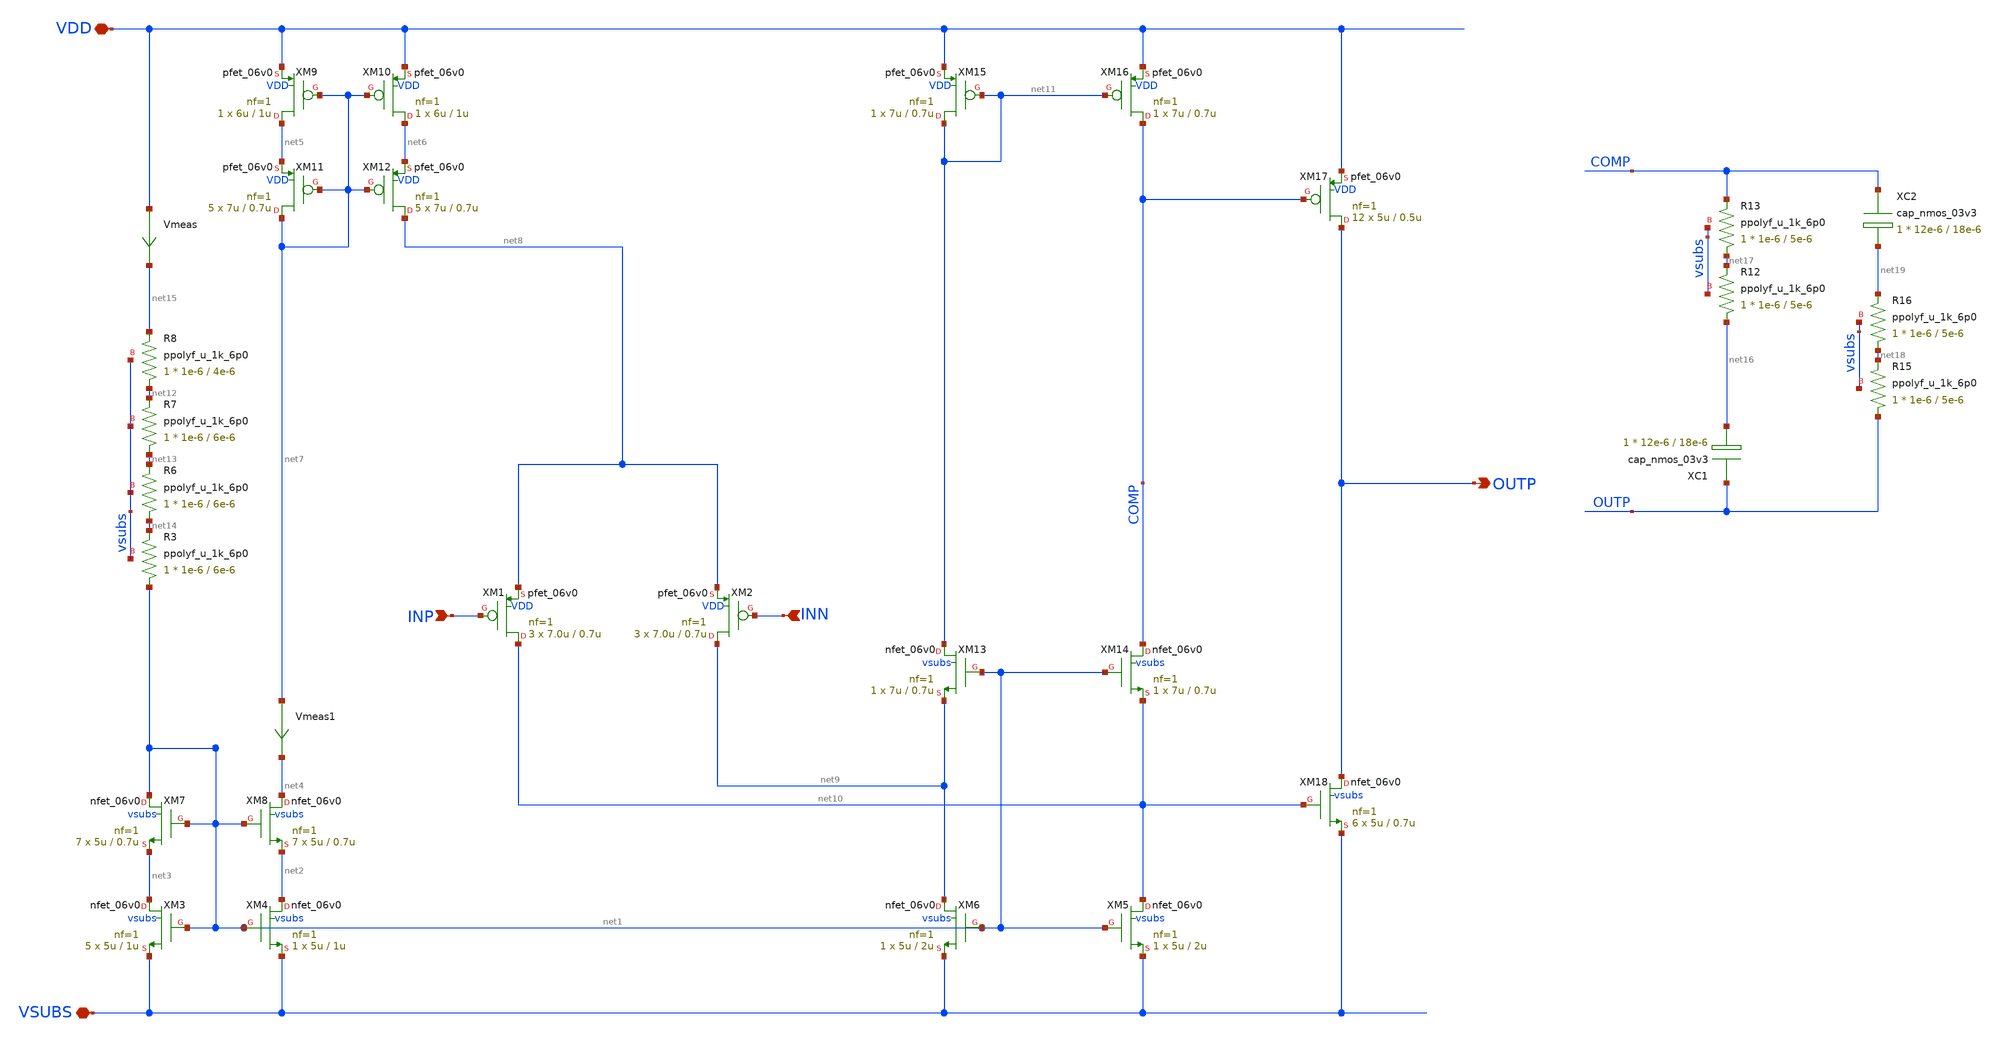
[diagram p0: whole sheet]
** sch_path: xschem/ip_amplifier.sch
**.subckt ip_amplifier VDD VSUBS INP INN OUTP
*.iopin VDD
*.iopin VSUBS
*.ipin INP
*.ipin INN
*.opin OUTP
XM1 net10 INP net8 VDD pfet_06v0 L=0.7u W=7.0u nf=1 ad='int((nf+1)/2) * W/nf * 0.18u' as='int((nf+2)/2) * W/nf * 0.18u'
+ pd='2*int((nf+1)/2) * (W/nf + 0.18u)' ps='2*int((nf+2)/2) * (W/nf + 0.18u)' nrd='0.18u / W' nrs='0.18u / W'
+ sa=0 sb=0 sd=0 m=3 par=3
XM2 net9 INN net8 VDD pfet_06v0 L=0.7u W=7.0u nf=1 ad='int((nf+1)/2) * W/nf * 0.18u' as='int((nf+2)/2) * W/nf * 0.18u'
+ pd='2*int((nf+1)/2) * (W/nf + 0.18u)' ps='2*int((nf+2)/2) * (W/nf + 0.18u)' nrd='0.18u / W' nrs='0.18u / W'
+ sa=0 sb=0 sd=0 m=3 par=3
XM5 net10 net1 VSUBS vsubs nfet_06v0 L=2u W=5u nf=1 ad='int((nf+1)/2) * W/nf * 0.18u' as='int((nf+2)/2) * W/nf * 0.18u'
+ pd='2*int((nf+1)/2) * (W/nf + 0.18u)' ps='2*int((nf+2)/2) * (W/nf + 0.18u)' nrd='0.18u / W' nrs='0.18u / W'
+ sa=0 sb=0 sd=0 m=1 par=1
XM6 net9 net1 VSUBS vsubs nfet_06v0 L=2u W=5u nf=1 ad='int((nf+1)/2) * W/nf * 0.18u' as='int((nf+2)/2) * W/nf * 0.18u'
+ pd='2*int((nf+1)/2) * (W/nf + 0.18u)' ps='2*int((nf+2)/2) * (W/nf + 0.18u)' nrd='0.18u / W' nrs='0.18u / W'
+ sa=0 sb=0 sd=0 m=1 par=1
XM3 net3 net1 VSUBS vsubs nfet_06v0 L=1u W=5u nf=1 ad='int((nf+1)/2) * W/nf * 0.18u' as='int((nf+2)/2) * W/nf * 0.18u'
+ pd='2*int((nf+1)/2) * (W/nf + 0.18u)' ps='2*int((nf+2)/2) * (W/nf + 0.18u)' nrd='0.18u / W' nrs='0.18u / W'
+ sa=0 sb=0 sd=0 m=5 par=5
XM4 net2 net1 VSUBS vsubs nfet_06v0 L=1u W=5u nf=1 ad='int((nf+1)/2) * W/nf * 0.18u' as='int((nf+2)/2) * W/nf * 0.18u'
+ pd='2*int((nf+1)/2) * (W/nf + 0.18u)' ps='2*int((nf+2)/2) * (W/nf + 0.18u)' nrd='0.18u / W' nrs='0.18u / W'
+ sa=0 sb=0 sd=0 m=1 par=1
XM7 net1 net1 net3 vsubs nfet_06v0 L=0.7u W=5u nf=1 ad='int((nf+1)/2) * W/nf * 0.18u' as='int((nf+2)/2) * W/nf * 0.18u'
+ pd='2*int((nf+1)/2) * (W/nf + 0.18u)' ps='2*int((nf+2)/2) * (W/nf + 0.18u)' nrd='0.18u / W' nrs='0.18u / W'
+ sa=0 sb=0 sd=0 m=7 par=7
XM8 net4 net1 net2 vsubs nfet_06v0 L=0.7u W=5u nf=1 ad='int((nf+1)/2) * W/nf * 0.18u' as='int((nf+2)/2) * W/nf * 0.18u'
+ pd='2*int((nf+1)/2) * (W/nf + 0.18u)' ps='2*int((nf+2)/2) * (W/nf + 0.18u)' nrd='0.18u / W' nrs='0.18u / W'
+ sa=0 sb=0 sd=0 m=7 par=7
XM9 net5 net7 VDD VDD pfet_06v0 L=1u W=6u nf=1 ad='int((nf+1)/2) * W/nf * 0.18u' as='int((nf+2)/2) * W/nf * 0.18u'
+ pd='2*int((nf+1)/2) * (W/nf + 0.18u)' ps='2*int((nf+2)/2) * (W/nf + 0.18u)' nrd='0.18u / W' nrs='0.18u / W'
+ sa=0 sb=0 sd=0 m=1 par=1
XM10 net6 net7 VDD VDD pfet_06v0 L=1u W=6u nf=1 ad='int((nf+1)/2) * W/nf * 0.18u' as='int((nf+2)/2) * W/nf * 0.18u'
+ pd='2*int((nf+1)/2) * (W/nf + 0.18u)' ps='2*int((nf+2)/2) * (W/nf + 0.18u)' nrd='0.18u / W' nrs='0.18u / W'
+ sa=0 sb=0 sd=0 m=1 par=1
XM11 net7 net7 net5 VDD pfet_06v0 L=0.7u W=7u nf=1 ad='int((nf+1)/2) * W/nf * 0.18u' as='int((nf+2)/2) * W/nf * 0.18u'
+ pd='2*int((nf+1)/2) * (W/nf + 0.18u)' ps='2*int((nf+2)/2) * (W/nf + 0.18u)' nrd='0.18u / W' nrs='0.18u / W'
+ sa=0 sb=0 sd=0 m=5 par=5
XM12 net8 net7 net6 VDD pfet_06v0 L=0.7u W=7u nf=1 ad='int((nf+1)/2) * W/nf * 0.18u' as='int((nf+2)/2) * W/nf * 0.18u'
+ pd='2*int((nf+1)/2) * (W/nf + 0.18u)' ps='2*int((nf+2)/2) * (W/nf + 0.18u)' nrd='0.18u / W' nrs='0.18u / W'
+ sa=0 sb=0 sd=0 m=5 par=5
XM13 net11 net1 net9 vsubs nfet_06v0 L=0.7u W=7u nf=1 ad='int((nf+1)/2) * W/nf * 0.18u' as='int((nf+2)/2) * W/nf * 0.18u'
+ pd='2*int((nf+1)/2) * (W/nf + 0.18u)' ps='2*int((nf+2)/2) * (W/nf + 0.18u)' nrd='0.18u / W' nrs='0.18u / W'
+ sa=0 sb=0 sd=0 m=1 par=1
XM14 COMP net1 net10 vsubs nfet_06v0 L=0.7u W=7u nf=1 ad='int((nf+1)/2) * W/nf * 0.18u' as='int((nf+2)/2) * W/nf * 0.18u'
+ pd='2*int((nf+1)/2) * (W/nf + 0.18u)' ps='2*int((nf+2)/2) * (W/nf + 0.18u)' nrd='0.18u / W' nrs='0.18u / W'
+ sa=0 sb=0 sd=0 m=1 par=1
XM15 net11 net11 VDD VDD pfet_06v0 L=0.7u W=7u nf=1 ad='int((nf+1)/2) * W/nf * 0.18u' as='int((nf+2)/2) * W/nf * 0.18u'
+ pd='2*int((nf+1)/2) * (W/nf + 0.18u)' ps='2*int((nf+2)/2) * (W/nf + 0.18u)' nrd='0.18u / W' nrs='0.18u / W'
+ sa=0 sb=0 sd=0 m=1 par=1
XM16 COMP net11 VDD VDD pfet_06v0 L=0.7u W=7u nf=1 ad='int((nf+1)/2) * W/nf * 0.18u' as='int((nf+2)/2) * W/nf * 0.18u'
+ pd='2*int((nf+1)/2) * (W/nf + 0.18u)' ps='2*int((nf+2)/2) * (W/nf + 0.18u)' nrd='0.18u / W' nrs='0.18u / W'
+ sa=0 sb=0 sd=0 m=1 par=1
XM17 OUTP COMP VDD VDD pfet_06v0 L=0.5u W=5u nf=1 ad='int((nf+1)/2) * W/nf * 0.18u' as='int((nf+2)/2) * W/nf * 0.18u'
+ pd='2*int((nf+1)/2) * (W/nf + 0.18u)' ps='2*int((nf+2)/2) * (W/nf + 0.18u)' nrd='0.18u / W' nrs='0.18u / W'
+ sa=0 sb=0 sd=0 m=12 par=12
XM18 OUTP net10 VSUBS vsubs nfet_06v0 L=0.7u W=5u nf=1 ad='int((nf+1)/2) * W/nf * 0.18u' as='int((nf+2)/2) * W/nf * 0.18u'
+ pd='2*int((nf+1)/2) * (W/nf + 0.18u)' ps='2*int((nf+2)/2) * (W/nf + 0.18u)' nrd='0.18u / W' nrs='0.18u / W'
+ sa=0 sb=0 sd=0 m=6 par=6
XR3 net1 net14 vsubs ppolyf_u_1k_6p0 r_width=1e-6 r_length=6e-6 m=1
XR6 net14 net13 vsubs ppolyf_u_1k_6p0 r_width=1e-6 r_length=6e-6 m=1
XR7 net13 net12 vsubs ppolyf_u_1k_6p0 r_width=1e-6 r_length=6e-6 m=1
XR8 net12 net15 vsubs ppolyf_u_1k_6p0 r_width=1e-6 r_length=4e-6 m=1
Vmeas VDD net15 0
Vmeas1 net7 net4 0
XC1 OUTP net16 cap_nmos_03v3 c_width=12e-6 c_length=18e-6 m=1
XC2 COMP net19 cap_nmos_03v3 c_width=12e-6 c_length=18e-6 m=1
XR12 net16 net17 vsubs ppolyf_u_1k_6p0 r_width=1e-6 r_length=5e-6 m=1
XR13 net17 COMP vsubs ppolyf_u_1k_6p0 r_width=1e-6 r_length=5e-6 m=1
XR15 OUTP net18 vsubs ppolyf_u_1k_6p0 r_width=1e-6 r_length=5e-6 m=1
XR16 net18 net19 vsubs ppolyf_u_1k_6p0 r_width=1e-6 r_length=5e-6 m=1
**.ends
.end
